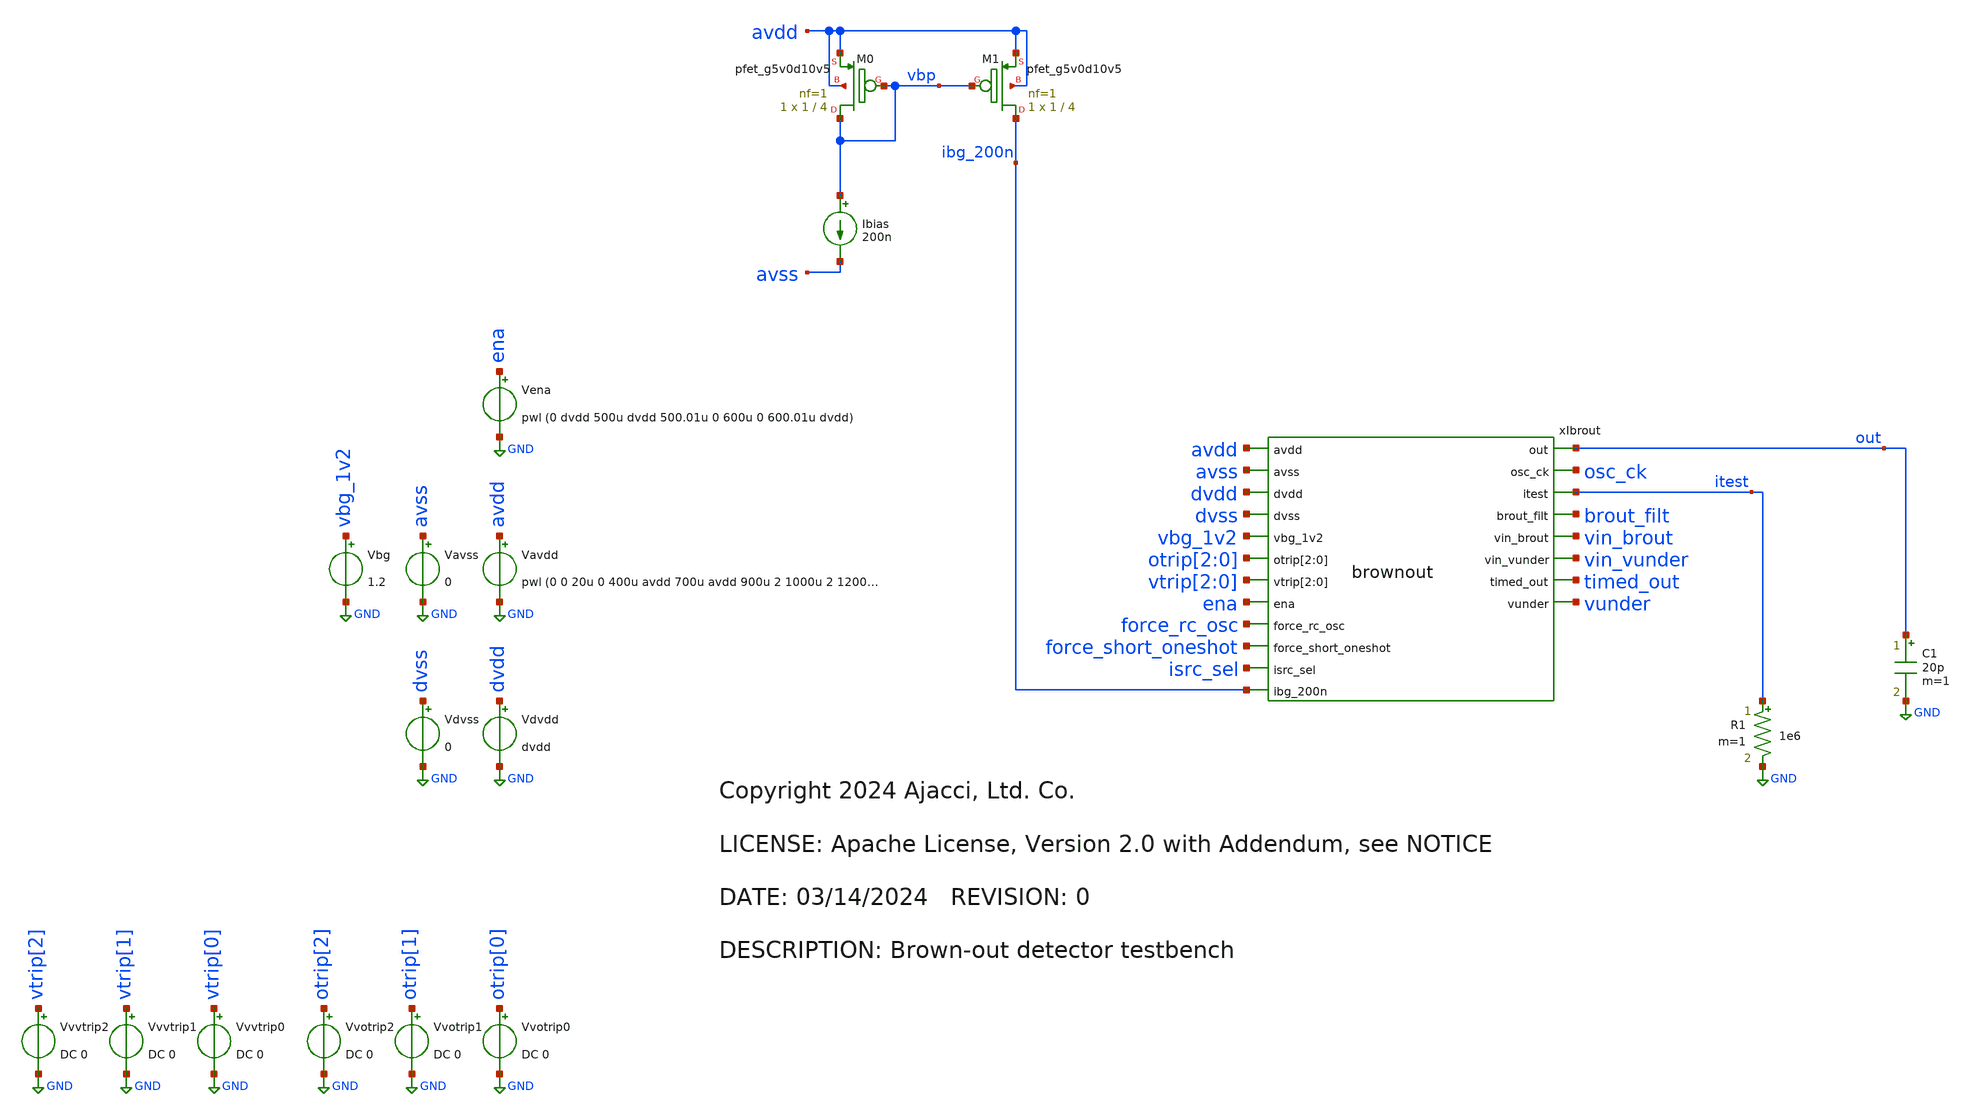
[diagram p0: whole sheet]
** sch_path: xschem/tb_brownout.sch
* Copyright 2024 Ajacci, Ltd. Co.
* LICENSE: Apache License, Version 2.0 with Addendum, see NOTICE
**.subckt tb_brownout
Vavss avss GND 0
Vena ena GND pwl (0 dvdd 500u dvdd 500.01u 0 600u 0 600.01u dvdd)
Vavdd avdd GND pwl (0 0 20u 0 400u avdd 700u avdd 900u 2 1000u 2 1200u avdd)
.save i(vavdd)
Vbg vbg_1v2 GND 1.2
Ibias vbp avss 200n
XM1 ibg_200n vbp avdd avdd sky130_fd_pr__pfet_g5v0d10v5 L=4 W=1 nf=1 ad='int((nf+1)/2) * W/nf * 0.29'
+ as='int((nf+2)/2) * W/nf * 0.29' pd='2*int((nf+1)/2) * (W/nf + 0.29)' ps='2*int((nf+2)/2) * (W/nf + 0.29)'
+ nrd='0.29 / W' nrs='0.29 / W' sa=0 sb=0 sd=0 mult=1 m=1
XM0 vbp vbp avdd avdd sky130_fd_pr__pfet_g5v0d10v5 L=4 W=1 nf=1 ad='int((nf+1)/2) * W/nf * 0.29' as='int((nf+2)/2) * W/nf * 0.29'
+ pd='2*int((nf+1)/2) * (W/nf + 0.29)' ps='2*int((nf+2)/2) * (W/nf + 0.29)' nrd='0.29 / W' nrs='0.29 / W'
+ sa=0 sb=0 sd=0 mult=1 m=1
Vdvss dvss GND 0
Vdvdd dvdd GND dvdd
.save i(vdvdd)
R1 itest GND 1e6 m=1
C1 out GND 20p m=1
xIbrout avdd avss out dvdd dvss osc_ck vbg_1v2 otrip[2] otrip[1] otrip[0] itest brout_filt vtrip[2]
+ vtrip[1] vtrip[0] vin_brout ena force_rc_osc vin_vunder force_short_oneshot timed_out vunder isrc_sel
+ ibg_200n brownout
Vvotrip0 otrip[0] GND DC 0
.save i(vvotrip0)
Vvotrip1 otrip[1] GND DC 0
.save i(vvotrip1)
Vvotrip2 otrip[2] GND DC 0
.save i(vvotrip2)
Vvvtrip0 vtrip[0] GND DC 0
.save i(vvvtrip0)
Vvvtrip1 vtrip[1] GND DC 0
.save i(vvvtrip1)
Vvvtrip2 vtrip[2] GND DC 0
.save i(vvvtrip2)
**** begin user architecture code


.param avdd=3.3
.param dvdd=1.8

.lib libs.tech/ngspice/sky130.lib.spice tt
.include libs.ref/sky130_fd_sc_hvl/spice/sky130_fd_sc_hvl.spice
.include libs.ref/sky130_fd_sc_hd/spice/sky130_fd_sc_hd.spice

*dig pull up/down to set test bits
R000 ena dvdd 1e9
R001 force_rc_osc dvss 1e9
R002 force_short_oneshot dvdd 1e9
R003 isrc_sel dvss 1e9

.temp 25
.save all
.save @m.xibrout.xiana.xirsmux.xmena.msky130_fd_pr__nfet_g5v0d10v5[id]

.control
tran 10u 3m
plot brout_filt itest avdd ena vbg_1v2 vin_brout vin_vunder timed_out xibrout.xiana.dcomp
+ xibrout.xiana.dcomp_filt
plot i(Vavdd) i(Vdvdd)
plot @m.xibrout.xiana.xirsmux.xmena.msky130_fd_pr__nfet_g5v0d10v5[id]
plot out avdd vunder*0.75 ena*0.5
plot xibrout.osc_ena 1.25*out 1.75*brout_filt
plot brout_filt xibrout.xiana.dcomp xibrout.xiana.dcomp_filt
plot avdd 0.25*osc_ck 0.5*ena 0.75*brout_filt timed_out 1.25*out 1.5*vunder
plot osc_ck*0.5 xibrout.xiana.xiosc.in xibrout.xiana.xiosc.m xibrout.osc_ena*0.25 brout_filt
+ out*1.25
.endc


**** end user architecture code
**.ends
.GLOBAL GND
.end
